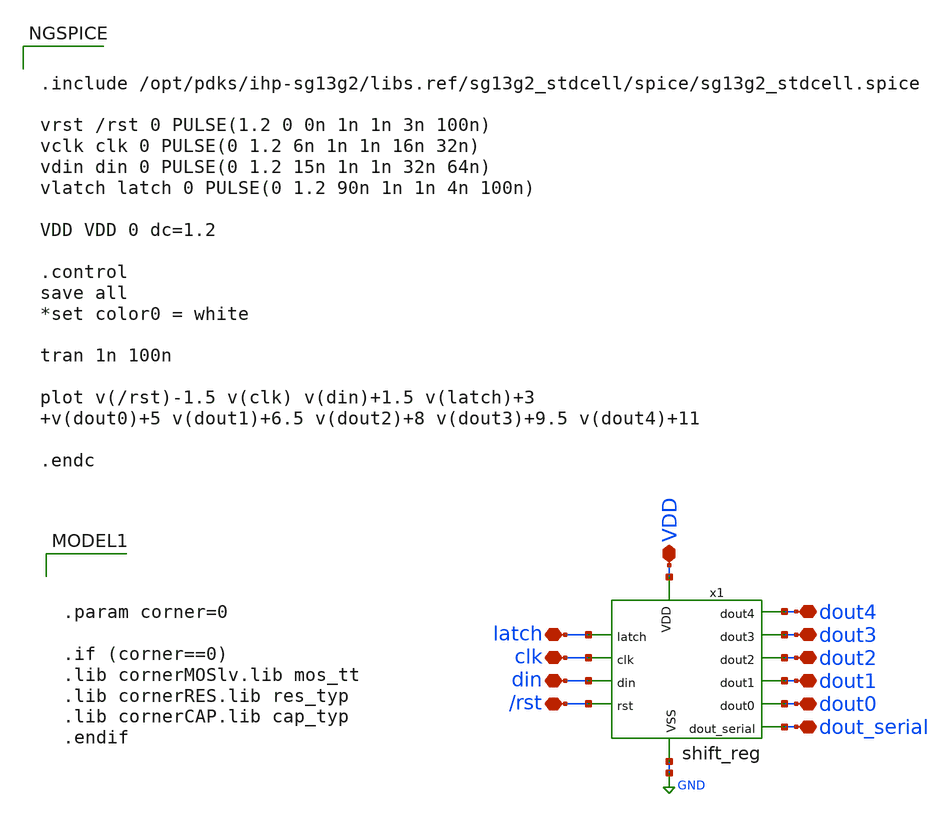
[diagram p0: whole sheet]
** sch_path: xschem/digital/tb_shift_reg.sch
**.subckt tb_shift_reg dout4 latch clk din /rst dout3 dout2 dout1 dout0 VDD dout_serial
*.iopin dout4
*.iopin latch
*.iopin clk
*.iopin din
*.iopin /rst
*.iopin dout3
*.iopin dout2
*.iopin dout1
*.iopin dout0
*.iopin VDD
*.iopin dout_serial
x1 dout4 dout2 dout1 dout3 dout0 VDD GND latch clk dout_serial din /rst shift_reg
**** begin user architecture code


.include /opt/pdks/ihp-sg13g2/libs.ref/sg13g2_stdcell/spice/sg13g2_stdcell.spice

vrst /rst 0 PULSE(1.2 0 0n 1n 1n 3n 100n)
vclk clk 0 PULSE(0 1.2 6n 1n 1n 16n 32n)
vdin din 0 PULSE(0 1.2 15n 1n 1n 32n 64n)
vlatch latch 0 PULSE(0 1.2 90n 1n 1n 4n 100n)

VDD VDD 0 dc=1.2

.control
save all
*set color0 = white

tran 1n 100n

plot v(/rst)-1.5 v(clk) v(din)+1.5 v(latch)+3 v(dout0)+5 v(dout1)+6.5 v(dout2)+8 v(dout3)+9.5
+ v(dout4)+11

.endc




.param corner=0

.if (corner==0)
.lib cornerMOSlv.lib mos_tt
.lib cornerRES.lib res_typ
.lib cornerCAP.lib cap_typ
.endif

**** end user architecture code
**.ends

* expanding   symbol:
*+  /home/designer/shared/ihp-sg13g2_ana_mux_32_1_serial_sel/src/digital/shift_reg.sym # of pins=12
** sym_path: src/digital/shift_reg.sym
** sch_path: src/digital/shift_reg.sch
.subckt shift_reg dout4 dout2 dout1 dout3 dout0 VDD VSS latch clk dout_serial din rst
*.ipin din
*.ipin rst
*.ipin clk
*.opin dout3
*.opin dout0
*.opin dout1
*.opin dout2
*.opin dout4
*.ipin latch
*.ipin VDD
*.ipin VSS
*.opin dout_serial
x1 din rst VGND VNB VPB VPWR net1 sg13g2_dlhrq_1
x2 net1 rst VGND VNB VPB VPWR net2 sg13g2_dlhrq_1
x3 net2 rst VGND VNB VPB VPWR net3 sg13g2_dlhrq_1
x4 net3 rst VGND VNB VPB VPWR net4 sg13g2_dlhrq_1
x5 net4 rst VGND VNB VPB VPWR dout_serial sg13g2_dlhrq_1
x6 net1 rst VGND VNB VPB VPWR dout4 sg13g2_dlhrq_1
x7 net2 rst VGND VNB VPB VPWR dout3 sg13g2_dlhrq_1
x8 net3 rst VGND VNB VPB VPWR dout2 sg13g2_dlhrq_1
x9 net4 rst VGND VNB VPB VPWR dout1 sg13g2_dlhrq_1
x10 dout_serial rst VGND VNB VPB VPWR dout0 sg13g2_dlhrq_1
.ends

.GLOBAL GND
.end
